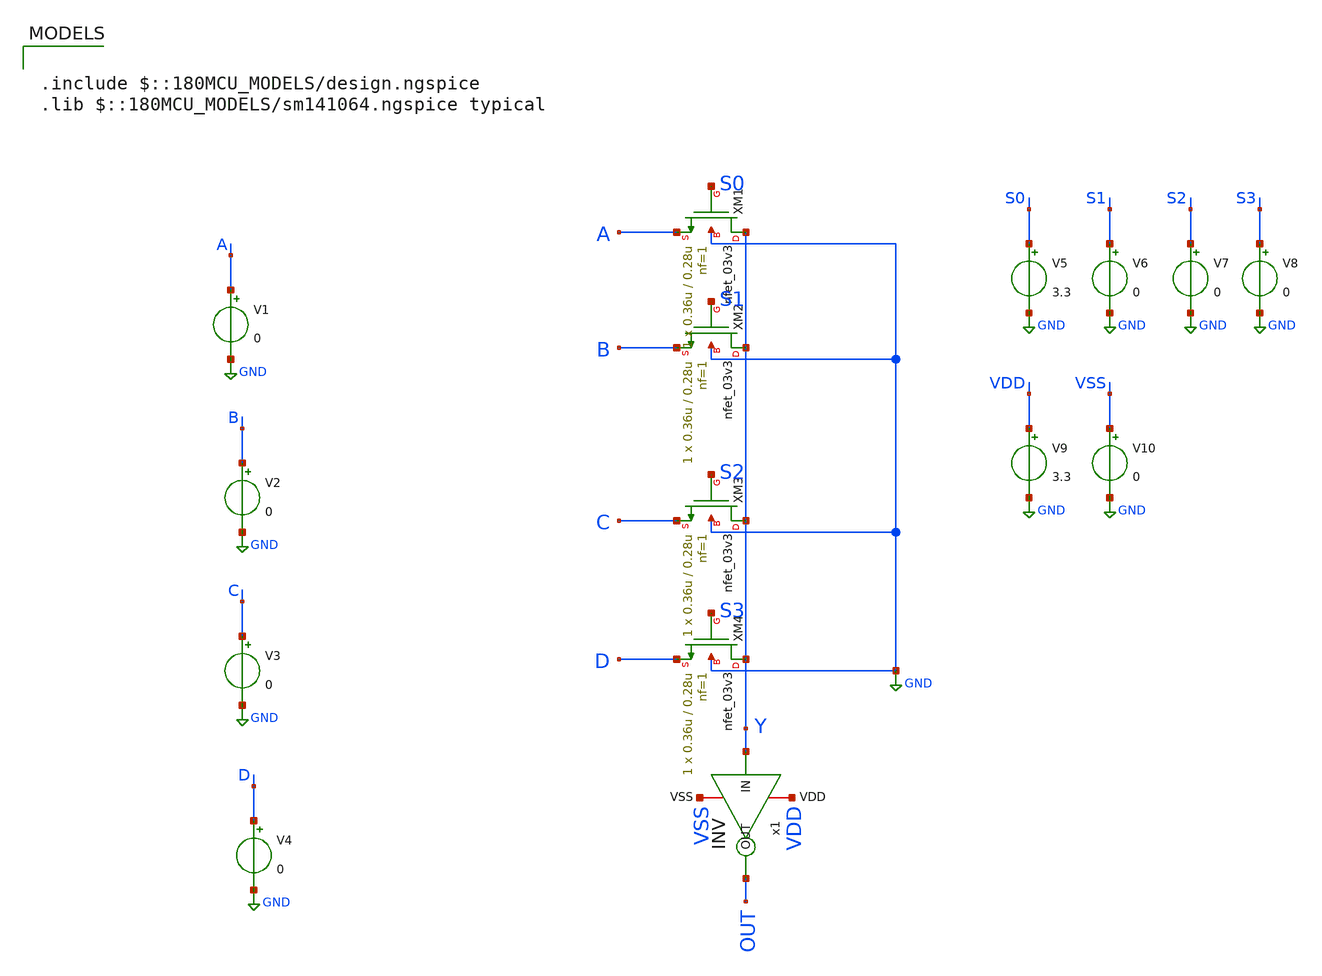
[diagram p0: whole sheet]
** sch_path: CAD4/4_pass_transisors.sch
**.subckt 4_pass_transisors
XM1 Y S0 A GND nfet_03v3 L=0.28u W=0.36u nf=1 ad='int((nf+1)/2) * W/nf * 0.18u' as='int((nf+2)/2) * W/nf * 0.18u'
+ pd='2*int((nf+1)/2) * (W/nf + 0.18u)' ps='2*int((nf+2)/2) * (W/nf + 0.18u)' nrd='0.18u / W' nrs='0.18u / W'
+ sa=0 sb=0 sd=0 m=1
XM2 Y S1 B GND nfet_03v3 L=0.28u W=0.36u nf=1 ad='int((nf+1)/2) * W/nf * 0.18u' as='int((nf+2)/2) * W/nf * 0.18u'
+ pd='2*int((nf+1)/2) * (W/nf + 0.18u)' ps='2*int((nf+2)/2) * (W/nf + 0.18u)' nrd='0.18u / W' nrs='0.18u / W'
+ sa=0 sb=0 sd=0 m=1
XM3 Y S2 C GND nfet_03v3 L=0.28u W=0.36u nf=1 ad='int((nf+1)/2) * W/nf * 0.18u' as='int((nf+2)/2) * W/nf * 0.18u'
+ pd='2*int((nf+1)/2) * (W/nf + 0.18u)' ps='2*int((nf+2)/2) * (W/nf + 0.18u)' nrd='0.18u / W' nrs='0.18u / W'
+ sa=0 sb=0 sd=0 m=1
XM4 Y S3 D GND nfet_03v3 L=0.28u W=0.36u nf=1 ad='int((nf+1)/2) * W/nf * 0.18u' as='int((nf+2)/2) * W/nf * 0.18u'
+ pd='2*int((nf+1)/2) * (W/nf + 0.18u)' ps='2*int((nf+2)/2) * (W/nf + 0.18u)' nrd='0.18u / W' nrs='0.18u / W'
+ sa=0 sb=0 sd=0 m=1
V1 A GND 0
V2 B GND 0
V3 C GND 0
V4 D GND 0
V5 S0 GND 3.3
V6 S1 GND 0
V7 S2 GND 0
V8 S3 GND 0
x1 VDD Y OUT VSS INV
V9 VDD GND 3.3
V10 VSS GND 0
**** begin user architecture code

.include $::180MCU_MODELS/design.ngspice
.lib $::180MCU_MODELS/sm141064.ngspice typical



.control

** Timing
let f = 1e8
let T = 1/f
let PW = T/2
let QT = T/4

let tstop = 2 * T
let tstep = 0.001 * T

alter @V1[PULSE] = [ 0 3.3 $&PW 0 0 $&PW $&T 0 ]
tran $&tstep $&tstop

meas tran TPHL TRIG V(A) VAL=1.65 RISE=1 TARG V(OUT) VAL=1.65 FALL=1 TD=$&QT
meas tran TPLH TRIG V(A) VAL=1.65 FALL=1 TARG V(OUT) VAL=1.65 RISE=1 TD=$&QT

plot OUT Y+5 A+10

.endc




**** end user architecture code
**.ends
.GLOBAL GND
.end
